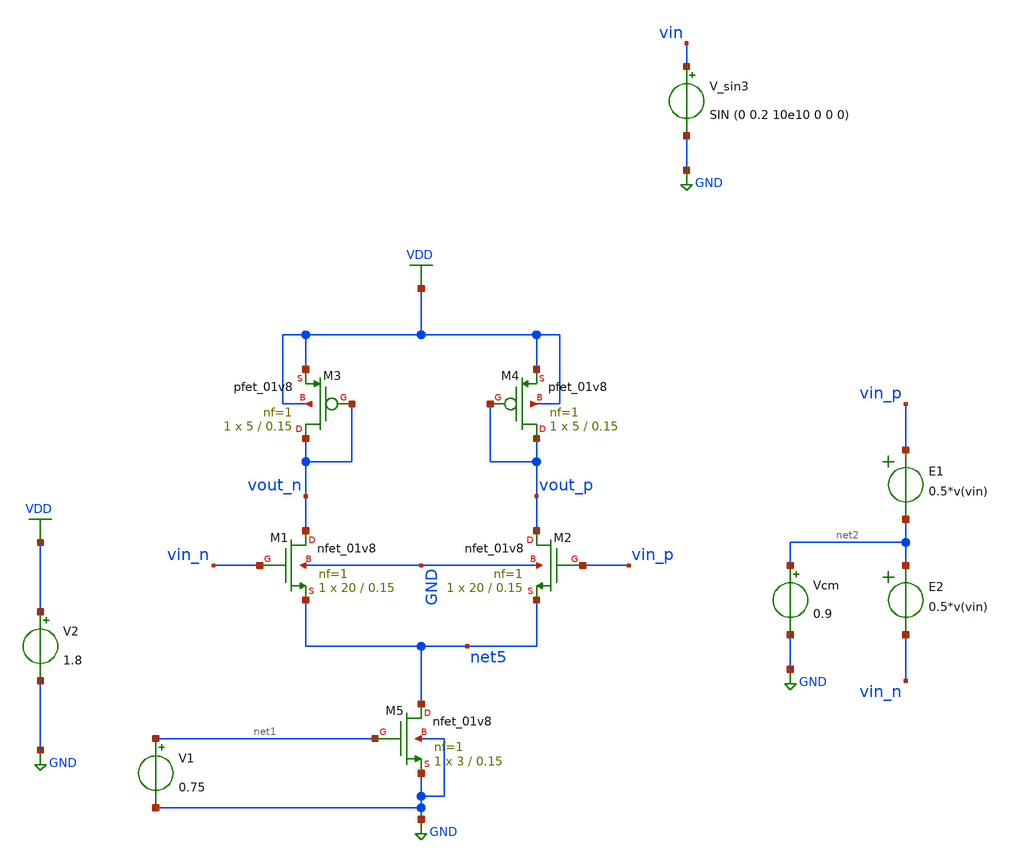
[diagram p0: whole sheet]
** sch_path: schem/amp.sch
**.subckt amp
XM2 vout_p vin_p net5 GND sky130_fd_pr__nfet_01v8 L=0.15 W=20 nf=1 ad='int((1 + 1)/2) * 20 / 1 * 0.29'
+ as='int((1 + 2)/2) * 20 / 1 * 0.29' pd='2*int((1 + 1)/2) * (20 / 1 + 0.29)' ps='2*int((1 + 2)/2) * (20 / 1 + 0.29)'
+ nrd='0.29 / 20 ' nrs='0.29 / 20 ' sa=0 sb=0 sd=0 mult=1 m=1
XM3 vout_n vout_n VDD VDD sky130_fd_pr__pfet_01v8 L=0.15 W=5 nf=1 ad='int((1 + 1)/2) * 5 / 1 * 0.29'
+ as='int((1 + 2)/2) * 5 / 1 * 0.29' pd='2*int((1 + 1)/2) * (5 / 1 + 0.29)' ps='2*int((1 + 2)/2) * (5 / 1 + 0.29)'
+ nrd='0.29 / 5 ' nrs='0.29 / 5 ' sa=0 sb=0 sd=0 mult=1 m=1
XM1 vout_n vin_n net5 GND sky130_fd_pr__nfet_01v8 L=0.15 W=20 nf=1 ad='int((1 + 1)/2) * 20 / 1 * 0.29'
+ as='int((1 + 2)/2) * 20 / 1 * 0.29' pd='2*int((1 + 1)/2) * (20 / 1 + 0.29)' ps='2*int((1 + 2)/2) * (20 / 1 + 0.29)'
+ nrd='0.29 / 20 ' nrs='0.29 / 20 ' sa=0 sb=0 sd=0 mult=1 m=1
XM4 vout_p vout_p VDD VDD sky130_fd_pr__pfet_01v8 L=0.15 W=5 nf=1 ad='int((1 + 1)/2) * 5 / 1 * 0.29'
+ as='int((1 + 2)/2) * 5 / 1 * 0.29' pd='2*int((1 + 1)/2) * (5 / 1 + 0.29)' ps='2*int((1 + 2)/2) * (5 / 1 + 0.29)'
+ nrd='0.29 / 5 ' nrs='0.29 / 5 ' sa=0 sb=0 sd=0 mult=1 m=1
XM5 net5 net1 GND GND sky130_fd_pr__nfet_01v8 L=0.15 W=3 nf=1 ad='int((1 + 1)/2) * 3 / 1 * 0.29' as='int((1 + 2)/2) * 3 / 1 * 0.29'
+ pd='2*int((1 + 1)/2) * (3 / 1 + 0.29)' ps='2*int((1 + 2)/2) * (3 / 1 + 0.29)' nrd='0.29 / 3 ' nrs='0.29 / 3 '
+ sa=0 sb=0 sd=0 mult=1 m=1
V1 net1 GND 0.75
Vcm net2 GND 0.9
V2 VDD GND 1.8
V_sin3 vin GND SIN (0 0.2 10e10 0 0 0)
E1 vin_p net2 VOL=' 0.5*v(vin) '
E2 net2 vin_n VOL=' 0.5*v(vin) '
**** begin user architecture code

.control
    save all
    +v(vin) v(vin_p) v(vin_n) v(vout_p) v(vout_n) v(net5)
    +@m.xm1.msky130_fd_pr__nfet_01v8[id] @m.xm1.msky130_fd_pr__nfet_01v8[gm]
    +@m.xm2.msky130_fd_pr__nfet_01v8[id] @m.xm2.msky130_fd_pr__nfet_01v8[gm]
    +@m.xm3.msky130_fd_pr__pfet_01v8[id] @m.xm3.msky130_fd_pr__pfet_01v8[gm]
    +@m.xm4.msky130_fd_pr__pfet_01v8[id] @m.xm4.msky130_fd_pr__pfet_01v8[gm]
    +@m.xm5.msky130_fd_pr__nfet_01v8[id] @m.xm5.msky130_fd_pr__nfet_01v8[gm]
    op
    write op.raw
    tran 1p 10n
    save all v(vi_i) v(vi_p) v(vi_n) v(vout_p)-v(vout_n)
    write tran.raw
.endc



** opencircuitdesign pdks install
.lib $::SKYWATER_MODELS/sky130.lib.spice tt

**** end user architecture code
**.ends
.GLOBAL VDD
.GLOBAL GND
.end
